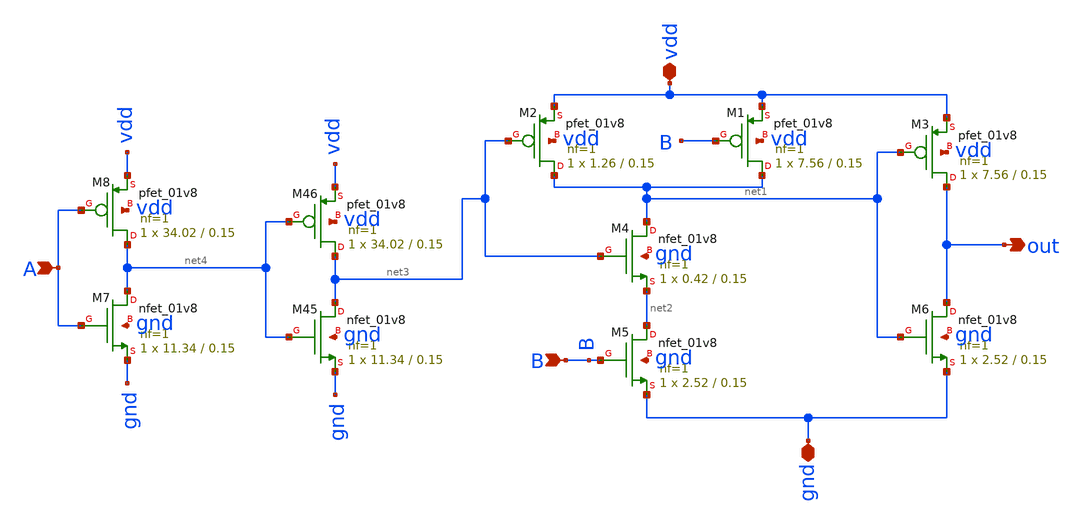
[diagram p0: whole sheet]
** sch_path: xschem/charge_pumps2/and_capacitor_8.sch
**.subckt and_capacitor_8 gnd vdd A B out
*.iopin gnd
*.iopin vdd
*.ipin A
*.ipin B
*.opin out
XM2 net1 net3 vdd vdd sky130_fd_pr__pfet_01v8 L=0.15 W=1.26 nf=1 ad='int((nf+1)/2) * W/nf * 0.29' as='int((nf+2)/2) * W/nf * 0.29'
+ pd='2*int((nf+1)/2) * (W/nf + 0.29)' ps='2*int((nf+2)/2) * (W/nf + 0.29)' nrd='0.29 / W' nrs='0.29 / W'
+ sa=0 sb=0 sd=0 mult=1 m=1
XM1 net1 B vdd vdd sky130_fd_pr__pfet_01v8 L=0.15 W=7.56 nf=1 ad='int((nf+1)/2) * W/nf * 0.29' as='int((nf+2)/2) * W/nf * 0.29'
+ pd='2*int((nf+1)/2) * (W/nf + 0.29)' ps='2*int((nf+2)/2) * (W/nf + 0.29)' nrd='0.29 / W' nrs='0.29 / W'
+ sa=0 sb=0 sd=0 mult=1 m=1
XM3 out net1 vdd vdd sky130_fd_pr__pfet_01v8 L=0.15 W=7.56 nf=1 ad='int((nf+1)/2) * W/nf * 0.29' as='int((nf+2)/2) * W/nf * 0.29'
+ pd='2*int((nf+1)/2) * (W/nf + 0.29)' ps='2*int((nf+2)/2) * (W/nf + 0.29)' nrd='0.29 / W' nrs='0.29 / W'
+ sa=0 sb=0 sd=0 mult=1 m=1
XM4 net1 net3 net2 gnd sky130_fd_pr__nfet_01v8 L=0.15 W=0.42 nf=1 ad='int((nf+1)/2) * W/nf * 0.29' as='int((nf+2)/2) * W/nf * 0.29'
+ pd='2*int((nf+1)/2) * (W/nf + 0.29)' ps='2*int((nf+2)/2) * (W/nf + 0.29)' nrd='0.29 / W' nrs='0.29 / W'
+ sa=0 sb=0 sd=0 mult=1 m=1
XM5 net2 B gnd gnd sky130_fd_pr__nfet_01v8 L=0.15 W=2.52 nf=1 ad='int((nf+1)/2) * W/nf * 0.29' as='int((nf+2)/2) * W/nf * 0.29'
+ pd='2*int((nf+1)/2) * (W/nf + 0.29)' ps='2*int((nf+2)/2) * (W/nf + 0.29)' nrd='0.29 / W' nrs='0.29 / W'
+ sa=0 sb=0 sd=0 mult=1 m=1
XM6 out net1 gnd gnd sky130_fd_pr__nfet_01v8 L=0.15 W=2.52 nf=1 ad='int((nf+1)/2) * W/nf * 0.29' as='int((nf+2)/2) * W/nf * 0.29'
+ pd='2*int((nf+1)/2) * (W/nf + 0.29)' ps='2*int((nf+2)/2) * (W/nf + 0.29)' nrd='0.29 / W' nrs='0.29 / W'
+ sa=0 sb=0 sd=0 mult=1 m=1
XM45 net3 net4 gnd gnd sky130_fd_pr__nfet_01v8 L=0.15 W=11.34 nf=1 ad='int((nf+1)/2) * W/nf * 0.29' as='int((nf+2)/2) * W/nf * 0.29'
+ pd='2*int((nf+1)/2) * (W/nf + 0.29)' ps='2*int((nf+2)/2) * (W/nf + 0.29)' nrd='0.29 / W' nrs='0.29 / W'
+ sa=0 sb=0 sd=0 mult=1 m=1
XM46 net3 net4 vdd vdd sky130_fd_pr__pfet_01v8 L=0.15 W=34.02 nf=1 ad='int((nf+1)/2) * W/nf * 0.29' as='int((nf+2)/2) * W/nf * 0.29'
+ pd='2*int((nf+1)/2) * (W/nf + 0.29)' ps='2*int((nf+2)/2) * (W/nf + 0.29)' nrd='0.29 / W' nrs='0.29 / W'
+ sa=0 sb=0 sd=0 mult=1 m=1
XM7 net4 A gnd gnd sky130_fd_pr__nfet_01v8 L=0.15 W=11.34 nf=1 ad='int((nf+1)/2) * W/nf * 0.29' as='int((nf+2)/2) * W/nf * 0.29'
+ pd='2*int((nf+1)/2) * (W/nf + 0.29)' ps='2*int((nf+2)/2) * (W/nf + 0.29)' nrd='0.29 / W' nrs='0.29 / W'
+ sa=0 sb=0 sd=0 mult=1 m=1
XM8 net4 A vdd vdd sky130_fd_pr__pfet_01v8 L=0.15 W=34.02 nf=1 ad='int((nf+1)/2) * W/nf * 0.29' as='int((nf+2)/2) * W/nf * 0.29'
+ pd='2*int((nf+1)/2) * (W/nf + 0.29)' ps='2*int((nf+2)/2) * (W/nf + 0.29)' nrd='0.29 / W' nrs='0.29 / W'
+ sa=0 sb=0 sd=0 mult=1 m=1
**.ends
.end
